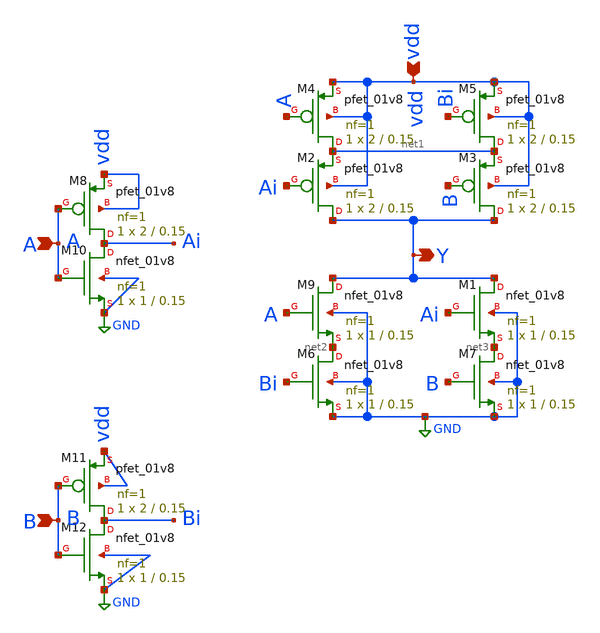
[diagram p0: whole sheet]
** sch_path: Circuit Files/Logic gate design using MOSFETS/gates/XNOR_GATE.sch
**.subckt XNOR_GATE Y A B vdd
*.opin Y
*.ipin A
*.ipin B
*.ipin vdd
XM2 Y Ai net1 vdd sky130_fd_pr__pfet_01v8 L=0.15 W=2 nf=1 ad='int((nf+1)/2) * W/nf * 0.29' as='int((nf+2)/2) * W/nf * 0.29'
+ pd='2*int((nf+1)/2) * (W/nf + 0.29)' ps='2*int((nf+2)/2) * (W/nf + 0.29)' nrd='0.29 / W' nrs='0.29 / W'
+ sa=0 sb=0 sd=0 mult=1 m=1
XM3 Y B net1 vdd sky130_fd_pr__pfet_01v8 L=0.15 W=2 nf=1 ad='int((nf+1)/2) * W/nf * 0.29' as='int((nf+2)/2) * W/nf * 0.29'
+ pd='2*int((nf+1)/2) * (W/nf + 0.29)' ps='2*int((nf+2)/2) * (W/nf + 0.29)' nrd='0.29 / W' nrs='0.29 / W'
+ sa=0 sb=0 sd=0 mult=1 m=1
XM4 net1 A vdd vdd sky130_fd_pr__pfet_01v8 L=0.15 W=2 nf=1 ad='int((nf+1)/2) * W/nf * 0.29' as='int((nf+2)/2) * W/nf * 0.29'
+ pd='2*int((nf+1)/2) * (W/nf + 0.29)' ps='2*int((nf+2)/2) * (W/nf + 0.29)' nrd='0.29 / W' nrs='0.29 / W'
+ sa=0 sb=0 sd=0 mult=1 m=1
XM5 net1 Bi vdd vdd sky130_fd_pr__pfet_01v8 L=0.15 W=2 nf=1 ad='int((nf+1)/2) * W/nf * 0.29' as='int((nf+2)/2) * W/nf * 0.29'
+ pd='2*int((nf+1)/2) * (W/nf + 0.29)' ps='2*int((nf+2)/2) * (W/nf + 0.29)' nrd='0.29 / W' nrs='0.29 / W'
+ sa=0 sb=0 sd=0 mult=1 m=1
XM9 Y A net2 GND sky130_fd_pr__nfet_01v8 L=0.15 W=1 nf=1 ad='int((nf+1)/2) * W/nf * 0.29' as='int((nf+2)/2) * W/nf * 0.29'
+ pd='2*int((nf+1)/2) * (W/nf + 0.29)' ps='2*int((nf+2)/2) * (W/nf + 0.29)' nrd='0.29 / W' nrs='0.29 / W'
+ sa=0 sb=0 sd=0 mult=1 m=1
XM1 Y Ai net3 GND sky130_fd_pr__nfet_01v8 L=0.15 W=1 nf=1 ad='int((nf+1)/2) * W/nf * 0.29' as='int((nf+2)/2) * W/nf * 0.29'
+ pd='2*int((nf+1)/2) * (W/nf + 0.29)' ps='2*int((nf+2)/2) * (W/nf + 0.29)' nrd='0.29 / W' nrs='0.29 / W'
+ sa=0 sb=0 sd=0 mult=1 m=1
XM6 net2 Bi GND GND sky130_fd_pr__nfet_01v8 L=0.15 W=1 nf=1 ad='int((nf+1)/2) * W/nf * 0.29' as='int((nf+2)/2) * W/nf * 0.29'
+ pd='2*int((nf+1)/2) * (W/nf + 0.29)' ps='2*int((nf+2)/2) * (W/nf + 0.29)' nrd='0.29 / W' nrs='0.29 / W'
+ sa=0 sb=0 sd=0 mult=1 m=1
XM7 net3 B GND GND sky130_fd_pr__nfet_01v8 L=0.15 W=1 nf=1 ad='int((nf+1)/2) * W/nf * 0.29' as='int((nf+2)/2) * W/nf * 0.29'
+ pd='2*int((nf+1)/2) * (W/nf + 0.29)' ps='2*int((nf+2)/2) * (W/nf + 0.29)' nrd='0.29 / W' nrs='0.29 / W'
+ sa=0 sb=0 sd=0 mult=1 m=1
XM8 Ai A vdd vdd sky130_fd_pr__pfet_01v8 L=0.15 W=2 nf=1 ad='int((nf+1)/2) * W/nf * 0.29' as='int((nf+2)/2) * W/nf * 0.29'
+ pd='2*int((nf+1)/2) * (W/nf + 0.29)' ps='2*int((nf+2)/2) * (W/nf + 0.29)' nrd='0.29 / W' nrs='0.29 / W'
+ sa=0 sb=0 sd=0 mult=1 m=1
XM10 Ai A GND GND sky130_fd_pr__nfet_01v8 L=0.15 W=1 nf=1 ad='int((nf+1)/2) * W/nf * 0.29' as='int((nf+2)/2) * W/nf * 0.29'
+ pd='2*int((nf+1)/2) * (W/nf + 0.29)' ps='2*int((nf+2)/2) * (W/nf + 0.29)' nrd='0.29 / W' nrs='0.29 / W'
+ sa=0 sb=0 sd=0 mult=1 m=1
XM11 Bi B vdd vdd sky130_fd_pr__pfet_01v8 L=0.15 W=2 nf=1 ad='int((nf+1)/2) * W/nf * 0.29' as='int((nf+2)/2) * W/nf * 0.29'
+ pd='2*int((nf+1)/2) * (W/nf + 0.29)' ps='2*int((nf+2)/2) * (W/nf + 0.29)' nrd='0.29 / W' nrs='0.29 / W'
+ sa=0 sb=0 sd=0 mult=1 m=1
XM12 Bi B GND GND sky130_fd_pr__nfet_01v8 L=0.15 W=1 nf=1 ad='int((nf+1)/2) * W/nf * 0.29' as='int((nf+2)/2) * W/nf * 0.29'
+ pd='2*int((nf+1)/2) * (W/nf + 0.29)' ps='2*int((nf+2)/2) * (W/nf + 0.29)' nrd='0.29 / W' nrs='0.29 / W'
+ sa=0 sb=0 sd=0 mult=1 m=1
**.ends
.GLOBAL GND
.end
